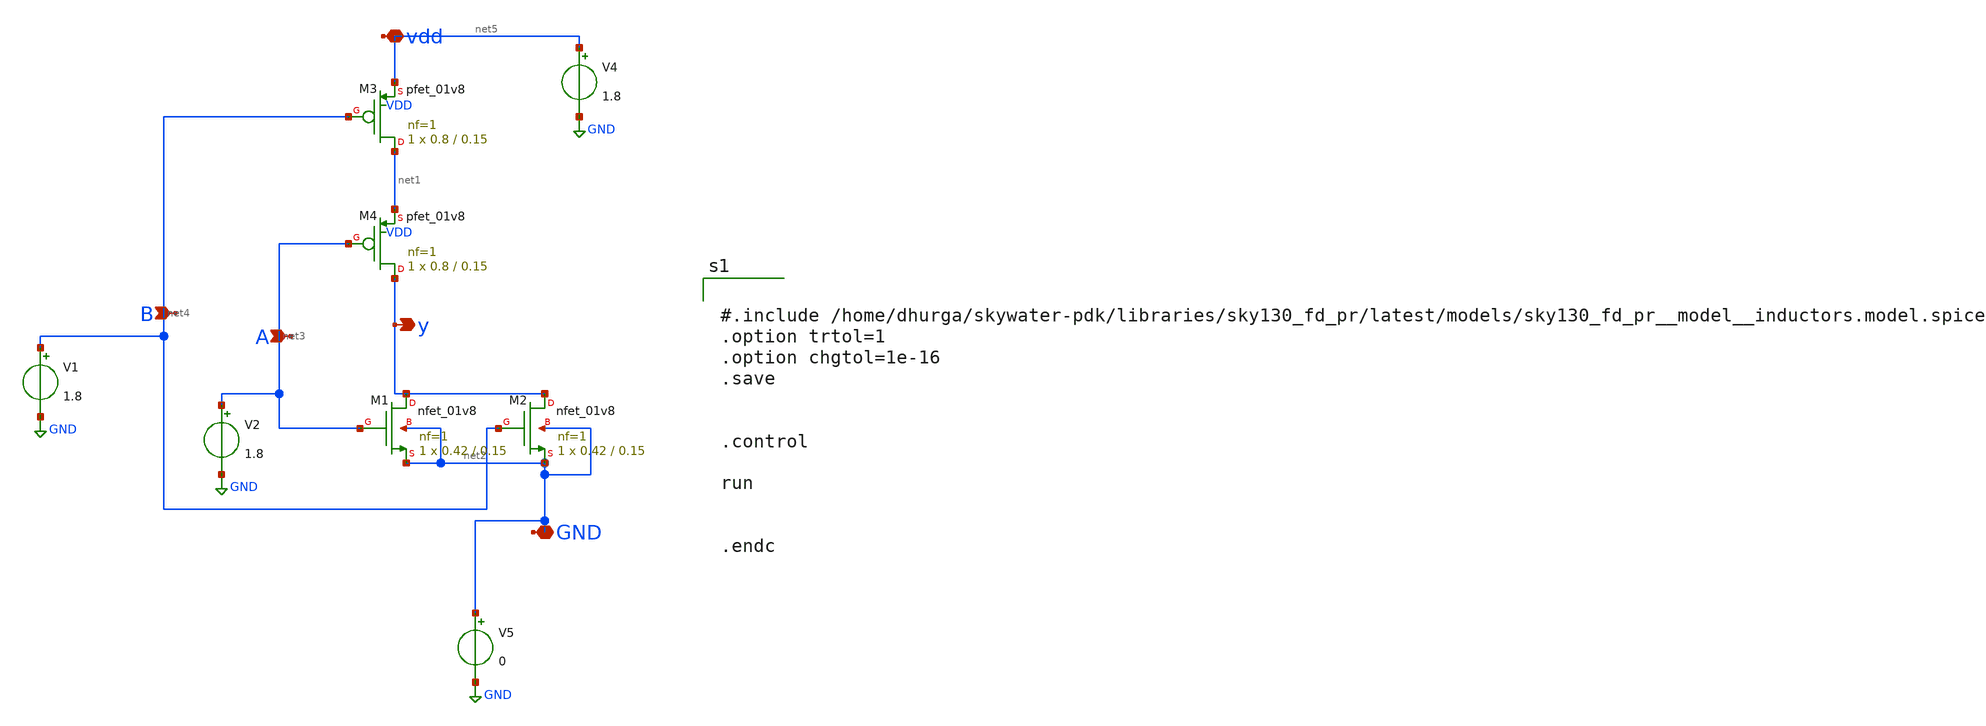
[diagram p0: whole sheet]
** sch_path: Xschem_ngspice_magic_netgen_caravel/nor_2in_xschem.sch
**.subckt nor_2in_xschem A B vdd y GND
*.ipin A
*.ipin B
*.iopin vdd
*.opin y
*.iopin GND
XM1 y net3 net2 net2 sky130_fd_pr__nfet_01v8 L=0.15 W=0.42 nf=1 ad='int((nf+1)/2) * W/nf * 0.29' as='int((nf+2)/2) * W/nf * 0.29'
+ pd='2*int((nf+1)/2) * (W/nf + 0.29)' ps='2*int((nf+2)/2) * (W/nf + 0.29)' nrd='0.29 / W' nrs='0.29 / W'
+ sa=0 sb=0 sd=0 mult=1 m=1
XM2 y net4 net2 net2 sky130_fd_pr__nfet_01v8 L=0.15 W=0.42 nf=1 ad='int((nf+1)/2) * W/nf * 0.29' as='int((nf+2)/2) * W/nf * 0.29'
+ pd='2*int((nf+1)/2) * (W/nf + 0.29)' ps='2*int((nf+2)/2) * (W/nf + 0.29)' nrd='0.29 / W' nrs='0.29 / W'
+ sa=0 sb=0 sd=0 mult=1 m=1
XM3 net1 net4 net5 VDD sky130_fd_pr__pfet_01v8 L=0.15 W=0.8 nf=1 ad='int((nf+1)/2) * W/nf * 0.29' as='int((nf+2)/2) * W/nf * 0.29'
+ pd='2*int((nf+1)/2) * (W/nf + 0.29)' ps='2*int((nf+2)/2) * (W/nf + 0.29)' nrd='0.29 / W' nrs='0.29 / W'
+ sa=0 sb=0 sd=0 mult=1 m=1
XM4 y net3 net1 VDD sky130_fd_pr__pfet_01v8 L=0.15 W=0.8 nf=1 ad='int((nf+1)/2) * W/nf * 0.29' as='int((nf+2)/2) * W/nf * 0.29'
+ pd='2*int((nf+1)/2) * (W/nf + 0.29)' ps='2*int((nf+2)/2) * (W/nf + 0.29)' nrd='0.29 / W' nrs='0.29 / W'
+ sa=0 sb=0 sd=0 mult=1 m=1
V1 net4 GND 1.8
V2 net3 GND 1.8
V4 net5 GND 1.8
V5 net2 GND 0
**** begin user architecture code



.lib /home/dhurga/open_pdks/sky130/sky130A/libs.tech/ngspice/sky130.lib.spice tt
#.include /home/dhurga/skywater-pdk/libraries/sky130_fd_pr/latest/models/sky130_fd_pr__model__inductors.model.spice
*.lib ~/open_pdks/sky130/sky130A/libs.tech/ngspice/sky130.lib.spice hh
* Resistor/Capacitor
*.include /home/dhurga/open_pdks/sky130/sky130A/libs.tech/ngspice/r+c/res_high__cap_high.spice
*.include /home/dhurga/open_pdks/sky130/sky130A/libs.tech/ngspice/r+c/res_high__cap_high__lin.spice
*.include /home/dhurga/open_pdks/sky130/sky130A/libs.tech/ngspice/corners/ff/specialized_cells.spice


*.include ~/open_pdks/sky130/sky130A/libs.tech/ngspice/corners/tt/nonfet.spice/wb_flat.spice



#.include /home/dhurga/skywater-pdk/libraries/sky130_fd_pr/latest/models/sky130_fd_pr__model__inductors.model.spice
.option trtol=1
.option chgtol=1e-16
.save


.control

run


.endc


**** end user architecture code
**.ends
.GLOBAL GND
.end
